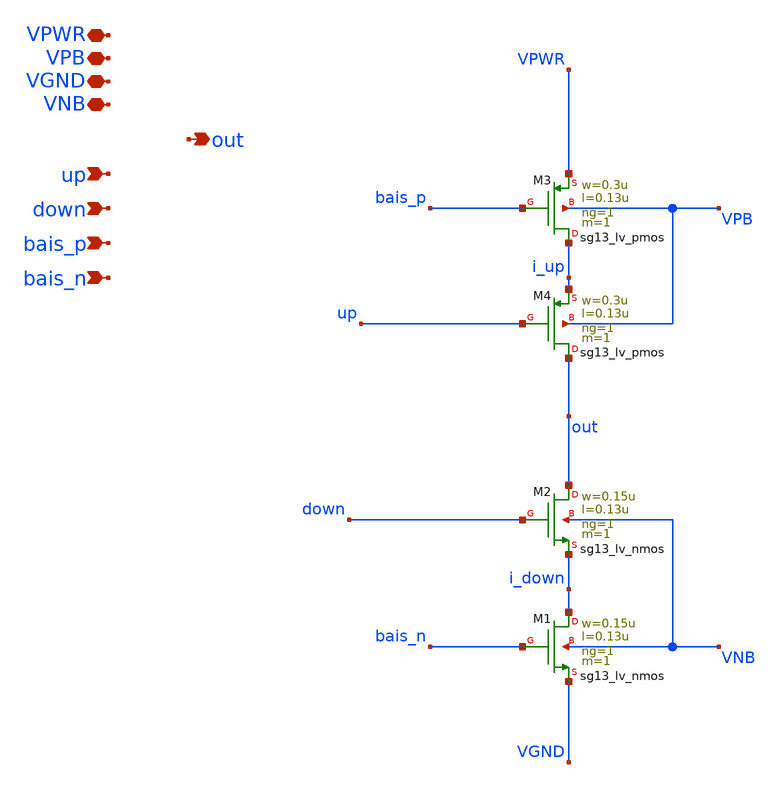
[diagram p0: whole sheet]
** sch_path: Team 2 Design/design_data/xschem/t2_charge_pump.sch
**.subckt t2_charge_pump VPWR up out VPB VGND VNB down bais_p bais_n
*.iopin VPWR
*.ipin up
*.opin out
*.iopin VPB
*.iopin VGND
*.iopin VNB
*.ipin down
*.ipin bais_p
*.ipin bais_n
XM1 i_down bais_n VGND VNB sg13_lv_nmos w=0.15u l=0.13u ng=1 m=1 mm_ok=1
XM2 out down i_down VNB sg13_lv_nmos w=0.15u l=0.13u ng=1 m=1 mm_ok=1
XM3 i_up bais_p VPWR VPB sg13_lv_pmos w=0.3u l=0.13u ng=1 m=1 mm_ok=1
XM4 out up i_up VPB sg13_lv_pmos w=0.3u l=0.13u ng=1 m=1 mm_ok=1
**.ends
.end
